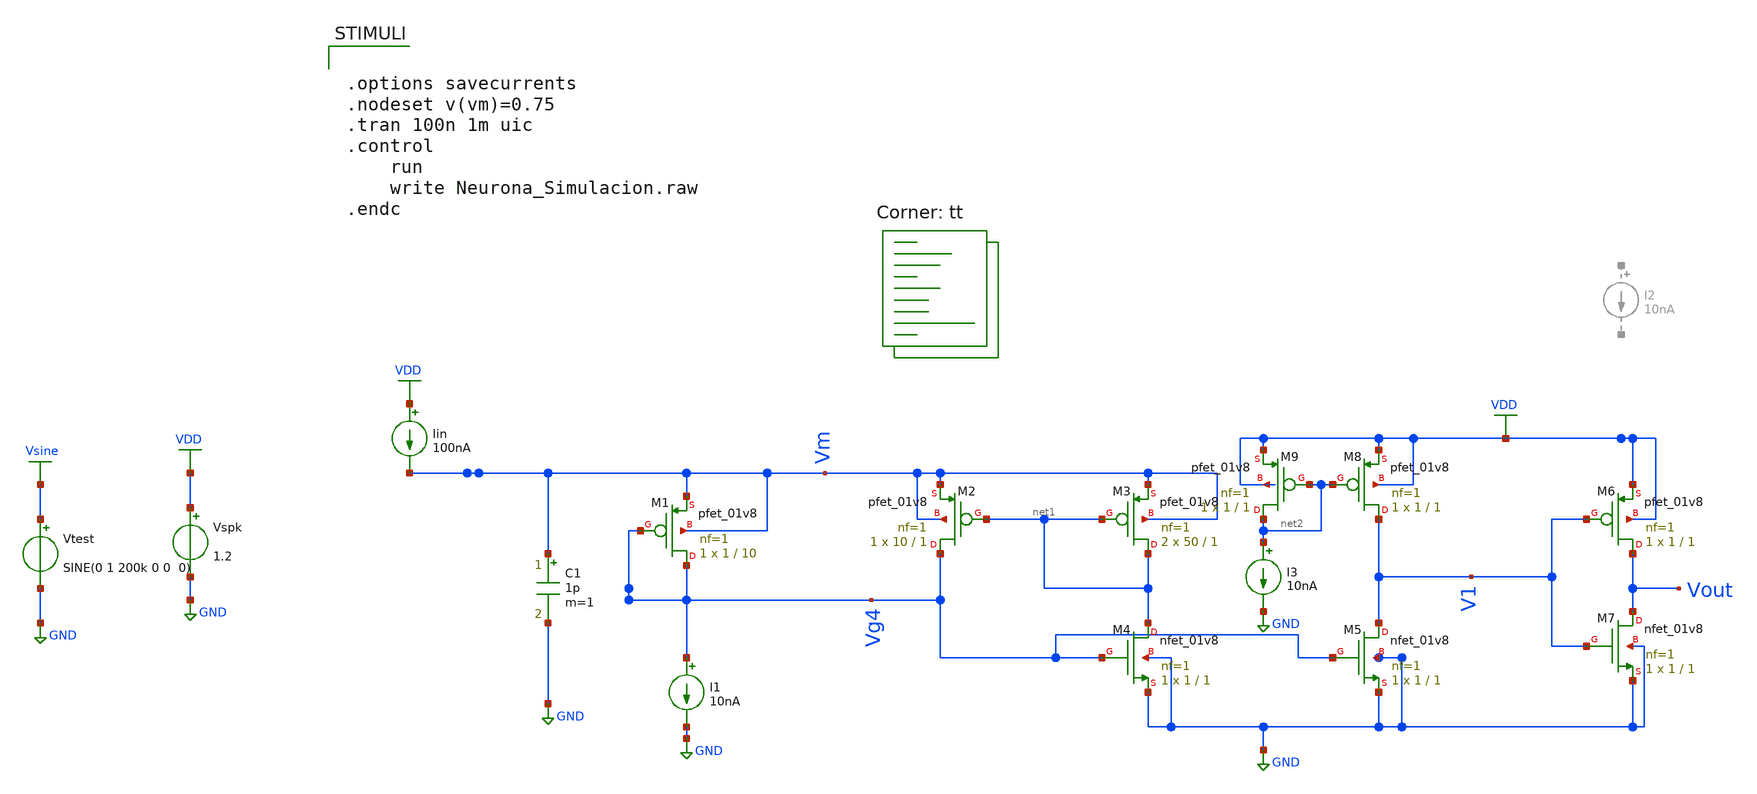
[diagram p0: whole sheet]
** sch_path: Neuron/ultralif/Neurona_Simulacion.sch
**.subckt Neurona_Simulacion
XM1 Vg4 Vg4 Vm Vm sky130_fd_pr__pfet_01v8 L=10 W=1 nf=1 ad='int((nf+1)/2) * W/nf * 0.29' as='int((nf+2)/2) * W/nf * 0.29'
+ pd='2*int((nf+1)/2) * (W/nf + 0.29)' ps='2*int((nf+2)/2) * (W/nf + 0.29)' nrd='0.29 / W' nrs='0.29 / W'
+ sa=0 sb=0 sd=0 mult=1 m=1
XM2 Vg4 net1 Vm Vm sky130_fd_pr__pfet_01v8 L=1 W=10 nf=1 ad='int((nf+1)/2) * W/nf * 0.29' as='int((nf+2)/2) * W/nf * 0.29'
+ pd='2*int((nf+1)/2) * (W/nf + 0.29)' ps='2*int((nf+2)/2) * (W/nf + 0.29)' nrd='0.29 / W' nrs='0.29 / W'
+ sa=0 sb=0 sd=0 mult=1 m=1
XM3 net1 net1 Vm Vm sky130_fd_pr__pfet_01v8 L=1 W=50 nf=1 ad='int((nf+1)/2) * W/nf * 0.29' as='int((nf+2)/2) * W/nf * 0.29'
+ pd='2*int((nf+1)/2) * (W/nf + 0.29)' ps='2*int((nf+2)/2) * (W/nf + 0.29)' nrd='0.29 / W' nrs='0.29 / W'
+ sa=0 sb=0 sd=0 mult=2 m=2
XM4 net1 Vg4 GND GND sky130_fd_pr__nfet_01v8 L=1 W=1 nf=1 ad='int((1 + 1)/2) * 1 / 1 * 0.29' as='int((1 + 2)/2) * 1 / 1 * 0.29'
+ pd='2*int((1 + 1)/2) * (1 / 1 + 0.29)' ps='2*int((1 + 2)/2) * (1 / 1 + 0.29)' nrd='0.29 / 1 ' nrs='0.29 / 1 '
+ sa=0 sb=0 sd=0 mult=1 m=1
XM5 V1 Vg4 GND GND sky130_fd_pr__nfet_01v8 L=1 W=1 nf=1 ad='int((1 + 1)/2) * 1 / 1 * 0.29' as='int((1 + 2)/2) * 1 / 1 * 0.29'
+ pd='2*int((1 + 1)/2) * (1 / 1 + 0.29)' ps='2*int((1 + 2)/2) * (1 / 1 + 0.29)' nrd='0.29 / 1 ' nrs='0.29 / 1 '
+ sa=0 sb=0 sd=0 mult=1 m=1
XM6 Vout V1 VDD VDD sky130_fd_pr__pfet_01v8 L=1 W=1 nf=1 ad='int((nf+1)/2) * W/nf * 0.29' as='int((nf+2)/2) * W/nf * 0.29'
+ pd='2*int((nf+1)/2) * (W/nf + 0.29)' ps='2*int((nf+2)/2) * (W/nf + 0.29)' nrd='0.29 / W' nrs='0.29 / W'
+ sa=0 sb=0 sd=0 mult=1 m=1
XM7 Vout V1 GND GND sky130_fd_pr__nfet_01v8 L=1 W=1 nf=1 ad='int((1 + 1)/2) * 1 / 1 * 0.29' as='int((1 + 2)/2) * 1 / 1 * 0.29'
+ pd='2*int((1 + 1)/2) * (1 / 1 + 0.29)' ps='2*int((1 + 2)/2) * (1 / 1 + 0.29)' nrd='0.29 / 1 ' nrs='0.29 / 1 '
+ sa=0 sb=0 sd=0 mult=1 m=1
I1 Vg4 GND 10nA
Vspk VDD GND 1.2
C1 Vm GND 1p m=1
Iin VDD Vm 100nA
XM8 V1 net2 VDD VDD sky130_fd_pr__pfet_01v8 L=1 W=1 nf=1 ad='int((nf+1)/2) * W/nf * 0.29' as='int((nf+2)/2) * W/nf * 0.29'
+ pd='2*int((nf+1)/2) * (W/nf + 0.29)' ps='2*int((nf+2)/2) * (W/nf + 0.29)' nrd='0.29 / W' nrs='0.29 / W'
+ sa=0 sb=0 sd=0 mult=1 m=1
XM9 net2 net2 VDD VDD sky130_fd_pr__pfet_01v8 L=1 W=1 nf=1 ad='int((nf+1)/2) * W/nf * 0.29' as='int((nf+2)/2) * W/nf * 0.29'
+ pd='2*int((nf+1)/2) * (W/nf + 0.29)' ps='2*int((nf+2)/2) * (W/nf + 0.29)' nrd='0.29 / W' nrs='0.29 / W'
+ sa=0 sb=0 sd=0 mult=1 m=1
I3 net2 GND 10nA
Vtest Vsine GND SINE(0 1 200k 0 0 0)
**** begin user architecture code
.lib $::SKYWATER_MODELS/sky130.lib.spice tt
**** end user architecture code
**.ends
.GLOBAL GND
.GLOBAL VDD
.GLOBAL Vsine
**** begin user architecture code


.options savecurrents
.nodeset v(vm)=0.75
.tran 100n 1m uic
.control
	run
	write Neurona_Simulacion.raw
.endc


**** end user architecture code
.end
